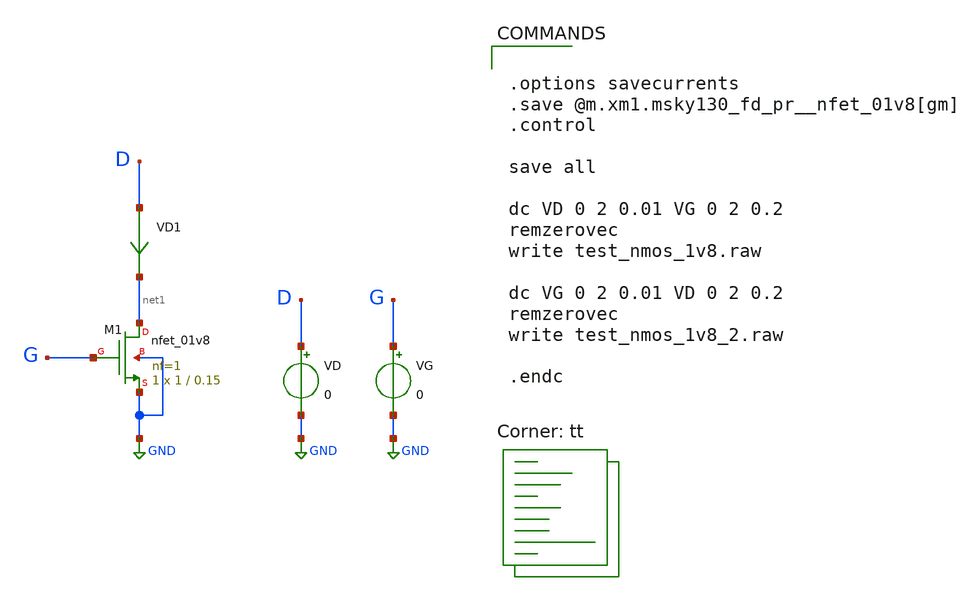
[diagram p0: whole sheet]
** sch_path: strongARM/test_nmos_1v8.sch
**.subckt test_nmos_1v8
VG G GND 0
VD D GND 0
VD1 D net1 0
.save i(vd1)
XM1 net1 G GND GND sky130_fd_pr__nfet_01v8 L=0.15 W=1 nf=1 ad='int((nf+1)/2) * W/nf * 0.29' as='int((nf+2)/2) * W/nf * 0.29'
+ pd='2*int((nf+1)/2) * (W/nf + 0.29)' ps='2*int((nf+2)/2) * (W/nf + 0.29)' nrd='0.29 / W' nrs='0.29 / W'
+ sa=0 sb=0 sd=0 mult=1 m=1
**** begin user architecture code
.lib $::SKYWATER_MODELS/sky130.lib.spice tt


.options savecurrents
.save @m.xm1.msky130_fd_pr__nfet_01v8[gm]
.control

save all

dc VD 0 2 0.01 VG 0 2 0.2
remzerovec
write test_nmos_1v8.raw

dc VG 0 2 0.01 VD 0 2 0.2
remzerovec
write test_nmos_1v8_2.raw

.endc


**** end user architecture code
**.ends
.GLOBAL GND
.end
